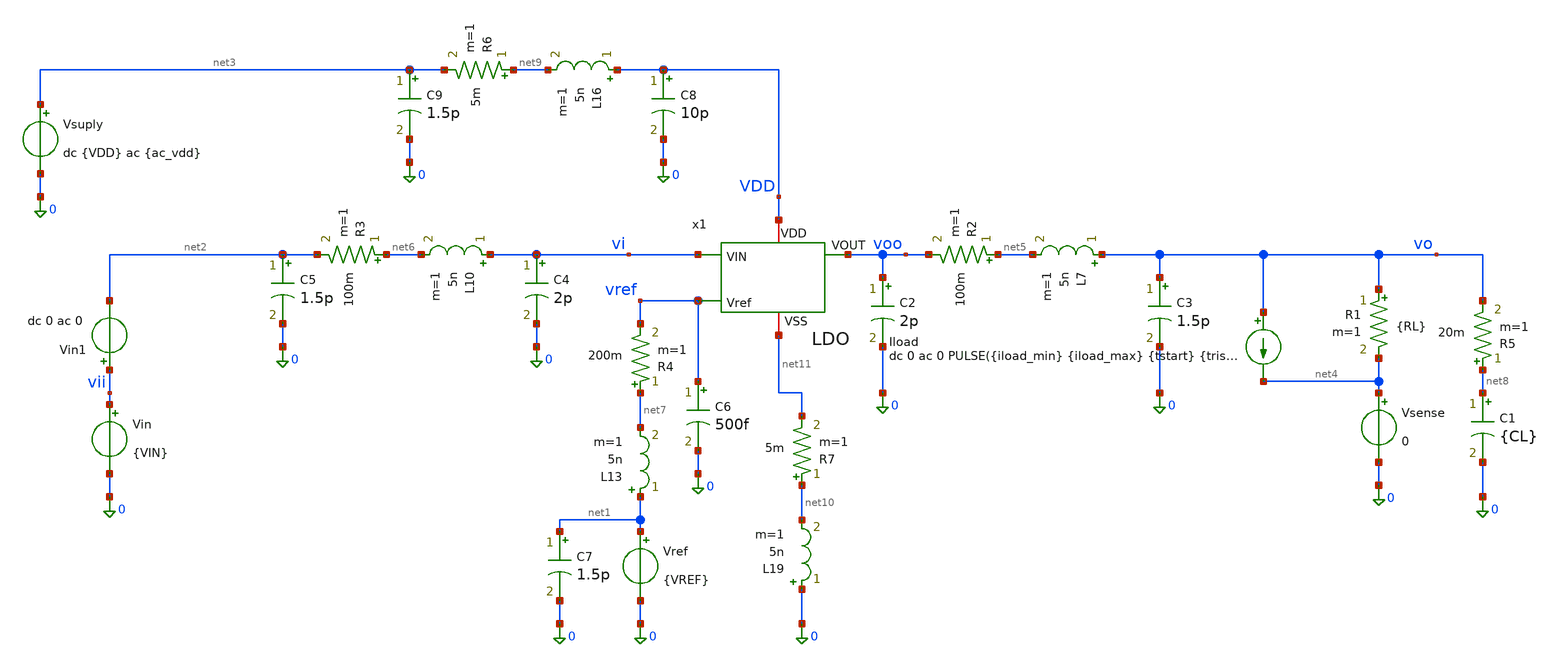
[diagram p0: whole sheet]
** sch_path: xschem/LDO_Top/ldo_tb.sch
**.subckt ldo_tb
Vsuply net3 0 dc {VDD} ac {ac_vdd}
Vref net1 0 {VREF}
Vin vii 0 {VIN}
R1 vo net4 {RL} m=1
C1 net8 0 {CL} m=1
Iload vo net4 dc 0 ac 0 PULSE({iload_min} {iload_max} {tstart} {trise} {tfall} {twidth} {tperiod})
Vsense net4 0 0
Vin1 vii net2 dc 0 ac 0
x1 vi voo VDD vref net11 LDO
C2 voo 0 2p m=1
R2 net5 voo 100m m=1
L7 vo net5 5n m=1
C3 vo 0 1.5p m=1
L10 vi net6 5n m=1
C4 vi 0 2p m=1
C5 net2 0 1.5p m=1
R3 net6 net2 100m m=1
L13 net1 net7 5n m=1
R4 net7 vref 200m m=1
C6 vref 0 500f m=1
C7 net1 0 1.5p m=1
R5 net8 vo 20m m=1
L16 VDD net9 5n m=1
C8 VDD 0 10p m=1
C9 net3 0 1.5p m=1
R6 net9 net3 5m m=1
L19 0 net10 5n m=1
R7 net10 net11 5m m=1
**** begin user architecture code









.lib /foss/pdks/sky130A/libs.tech/ngspice/sky130.lib.spice ff_lh
.option temp=-40
.param VDD = 1.98

.option num_threads=8

.param rsh_var = agauss(0, 0.005, 1)


* Forzar un punto de partida para ayudar a la convergencia
.nodeset V(VO)=1.2
.nodeset V(x1.Vre)=0.6




**parametros_ldo

.param VREF = 0.6
.param VIN = '1*VDD-0.3'
.param RL = 1200
.param CL = 1u
.param tsim = 2m

* Parámetros para la prueba de carga del LDO
.param iload_min = 1u
.param iload_max = 5m
.param tstart   = 30u
.param trise    = 100n
.param tfall    = 100n
.param twidth   = 100u
.param tperiod  = 200u

.param tsim = '3*tperiod'

.param ac_iprobe = 1
.param ac_vdd = 0

* --- Clamp SOLO de simulación (evita soluciones DC falsas de cientos de V) ---
* Diodo a tierra: conduce si vo baja de -0.2 V
Dclpn 0 vo dclamp_tb
* Diodo a una fuente de 5 V: conduce si vo sube de 5.7 V
Dclpp vo vclp dclamp_tb
* Fuente de referencia para el clamp superior
Dclpn2 0 x1.vre dclamp_tb
Dclpp2 x1.vre vclp dclamp_tb
Vclp vclp 0 5
* Modelo del diodo (fuga ~fA, sin capacitancia: no altera AC ni transitorio)
.model dclamp_tb D(IS=1e-15 N=1)









.control
let tperiod  = 200u
let tsim = '3*tperiod'


* =========================================================
* 2. AC (Estabilidad) -> Genera plot ac1
* =========================================================

ac dec 10 1 1G


let T_loop = v(x1.vre) / v(x1.vre2)
let ldb = vdb(T_loop)
let fase = vp(T_loop) * 180 / pi

write LDO_ac_estability.raw
meas ac ugb WHEN ldb = 0.0
meas ac fase_ugb FIND fase WHEN ldb = 0.0
let margen_fase = fase_ugb
meas ac ganancia_banda_plana find ldb at=1

* =========================================================
* 3. AC (PSRR) -> Genera plot ac2
* =========================================================
alterparam ac_iprobe = 0
alterparam ac_vdd = 1
reset

ac dec 10 10 1G


let psrr1 = v(vdd)/v(vo)
let psrr_db = vdb(psrr1)
write LDO_ac_psrr.raw
meas ac gananciaPSRR_1   find psrr_db at=10
meas ac gananciaPSRR_1k  find psrr_db at=1k
meas ac gananciaPSRR_10k find psrr_db at=10k
meas ac gananciaPSRR_1M  find psrr_db at=1Meg

* =========================================================
* 4. TRANSIENTE (Line Regulation) -> Genera plot tran1
* =========================================================
alterparam ac_iprobe = 0
alterparam ac_vdd = 0
reset

alter @Vin[pwl] = [ 0 1.4 1m 1.8 ]
alter @Iload[pwl] = [ 0 1u 1m 1u ]

tran 1u 1m
write LDO_dc_line.raw

let t_line_ini = 40u
let t_line_fin = 950u

meas tran voline_max MAX v(vo) from=$&t_line_ini to=$&t_line_fin
meas tran voline_min MIN v(vo) from=$&t_line_ini to=$&t_line_fin
let line_regulation_mV = (voline_max - voline_min)*1000
meas tran salida_line avg v(vo) from=$&t_line_ini to=$&t_line_fin
* =========================================================

* 1. TRANSIENTE (Overshoot y Undershoot) -> Genera plot tran2
* =========================================================
alterparam ac_iprobe = 0
alterparam ac_vdd = 0
alterparam RL = 240e9
reset

tran 1u $&tsim
write LDO_tran_picos.raw

let t_ignorar = 150u

meas tran v_estable_ligera FIND v(vo) AT=270u
meas tran v_estable_pesada FIND v(vo) AT=180u
meas tran vo_max MAX v(vo) from=$&t_ignorar to=$&tsim
meas tran vo_min MIN v(vo) from=$&t_ignorar to=$&tsim

let undershoot_mV = (v_estable_ligera - vo_min) * 1e3
let overshoot_mV = (vo_max - v_estable_pesada) * 1e3
meas tran salida_tran avg v(vo) from=$&t_ignorar to=$&tsim


* =========================================================
* 5. TRANSIENTE (Load Regulation) -> Genera plot tran3
* =========================================================
alterparam RL = 240e9
reset
alter @Iload[pwl] = [ 0 1u 1m 5m ]

tran 1u 1m
write LDO_dc_load.raw

meas tran vout_light FIND v(vo) AT=40u
meas tran vout_heavy FIND v(vo) AT=1m
let load_regulation_mV = (vout_light - vout_heavy) * 1000

* =========================================================
* 6. TRANSIENTE (Dropout) -> Genera plot tran4
* =========================================================
alterparam RL = 240
reset
alter @Vin[pwl] = [ 0 2 1m 0 ]
alter @Iload[pwl] = [ 0 1u 1m 1u ]

tran 1u 1m
write LDO_dc_dropout.raw

meas tran vout_nom FIND v(vo) AT=225u
let vout_target = vout_nom * 0.90
meas tran vin_do FIND v(vi) WHEN v(vo) = vout_target fall=1
let dropout_mV = (vin_do - vout_target) * 1e3

* =========================================================
* IMPRESION DE TODOS LOS RESULTADOS CON SETPLOT
* =========================================================

echo '--- RESULTADOS DE TRANSIENTE ---'
setplot tran3
print undershoot_mV overshoot_mV v_estable_ligera v_estable_pesada salida_tran

echo '--- RESULTADOS AC (ESTABILIDAD) ---'
setplot ac1
print ugb fase_ugb margen_fase ganancia_banda_plana

echo '--- RESULTADOS AC (PSRR) ---'
setplot ac2
print gananciaPSRR_1 gananciaPSRR_1k gananciaPSRR_10k gananciaPSRR_1M

echo '--- RESULTADOS REGULACIONES Y DROPOUT ---'
echo '>> Line Regulation'
setplot tran2
print line_regulation_mV salida_line

echo '>> Load Regulation'
setplot tran4
print load_regulation_mV

echo '>> Dropout'
setplot tran5
print dropout_mV vin_do vout_target

.endc






















.control



alterparam RL = 1200
alterparam ac_iprobe = 0
alterparam ac_vdd = 0

reset

*  Punto de Operación (.OP)

save all


save @m.x1.xM1.msky130_fd_pr__pfet_01v8_lvt[gm]
save @m.x1.xM1.msky130_fd_pr__pfet_01v8_lvt[gds]
save @m.x1.xM1.msky130_fd_pr__pfet_01v8_lvt[id]
save @m.x1.xM1.msky130_fd_pr__pfet_01v8_lvt[vgs]
save @m.x1.xM1.msky130_fd_pr__pfet_01v8_lvt[vds]
save @m.x1.xM1.msky130_fd_pr__pfet_01v8_lvt[vth]
save @m.x1.xM1.msky130_fd_pr__pfet_01v8_lvt[vdsat]




save @m.x1.x1.xMr.msky130_fd_pr__pfet_01v8_lvt[gm]
save @m.x1.x1.xMr.msky130_fd_pr__pfet_01v8_lvt[gds]
save @m.x1.x1.xMr.msky130_fd_pr__pfet_01v8_lvt[id]
save @m.x1.x1.xMr.msky130_fd_pr__pfet_01v8_lvt[vgs]
save @m.x1.x1.xMr.msky130_fd_pr__pfet_01v8_lvt[vds]
save @m.x1.x1.xMr.msky130_fd_pr__pfet_01v8_lvt[vth]
save @m.x1.x1.xMr.msky130_fd_pr__pfet_01v8_lvt[vdsat]

save @m.x1.x1.xMnref.msky130_fd_pr__nfet_01v8[gm]
save @m.x1.x1.xMnref.msky130_fd_pr__nfet_01v8[gds]
save @m.x1.x1.xMnref.msky130_fd_pr__nfet_01v8[id]
save @m.x1.x1.xMnref.msky130_fd_pr__nfet_01v8[vgs]
save @m.x1.x1.xMnref.msky130_fd_pr__nfet_01v8[vds]
save @m.x1.x1.xMnref.msky130_fd_pr__nfet_01v8[vth]
save @m.x1.x1.xMnref.msky130_fd_pr__nfet_01v8[vdsat]

save @m.x1.xMnl.msky130_fd_pr__nfet_01v8[gm]
save @m.x1.xMnl.msky130_fd_pr__nfet_01v8[gds]
save @m.x1.xMnl.msky130_fd_pr__nfet_01v8[id]
save @m.x1.xMnl.msky130_fd_pr__nfet_01v8[vgs]
save @m.x1.xMnl.msky130_fd_pr__nfet_01v8[vds]
save @m.x1.xMnl.msky130_fd_pr__nfet_01v8[vth]
save @m.x1.xMnl.msky130_fd_pr__nfet_01v8[vdsat]



* --- Etapa Diferencial (Núcleo del OTA) ---

* Mrc1 (pfet_01v8_lvt)
save @m.x1.x1.xMrc1.msky130_fd_pr__pfet_01v8_lvt[gm]
save @m.x1.x1.xMrc1.msky130_fd_pr__pfet_01v8_lvt[gds]
save @m.x1.x1.xMrc1.msky130_fd_pr__pfet_01v8_lvt[id]
save @m.x1.x1.xMrc1.msky130_fd_pr__pfet_01v8_lvt[vgs]
save @m.x1.x1.xMrc1.msky130_fd_pr__pfet_01v8_lvt[vds]
save @m.x1.x1.xMrc1.msky130_fd_pr__pfet_01v8_lvt[vth]
save @m.x1.x1.xMrc1.msky130_fd_pr__pfet_01v8_lvt[vdsat]

* Mn (pfet_01v8)
save @m.x1.x1.xMn.msky130_fd_pr__pfet_01v8_lvt[gm]
save @m.x1.x1.xMn.msky130_fd_pr__pfet_01v8_lvt[gds]
save @m.x1.x1.xMn.msky130_fd_pr__pfet_01v8_lvt[id]
save @m.x1.x1.xMn.msky130_fd_pr__pfet_01v8_lvt[vgs]
save @m.x1.x1.xMn.msky130_fd_pr__pfet_01v8_lvt[vds]
save @m.x1.x1.xMn.msky130_fd_pr__pfet_01v8_lvt[vth]
save @m.x1.x1.xMn.msky130_fd_pr__pfet_01v8_lvt[vdsat]

* Mp (pfet_01v8)
save @m.x1.x1.xMp.msky130_fd_pr__pfet_01v8_lvt[gm]
save @m.x1.x1.xMp.msky130_fd_pr__pfet_01v8_lvt[gds]
save @m.x1.x1.xMp.msky130_fd_pr__pfet_01v8_lvt[id]
save @m.x1.x1.xMp.msky130_fd_pr__pfet_01v8_lvt[vgs]
save @m.x1.x1.xMp.msky130_fd_pr__pfet_01v8_lvt[vds]
save @m.x1.x1.xMp.msky130_fd_pr__pfet_01v8_lvt[vth]
save @m.x1.x1.xMp.msky130_fd_pr__pfet_01v8_lvt[vdsat]

* Mnr (nfet_01v8)
save @m.x1.x1.xMnr.msky130_fd_pr__nfet_01v8[gm]
save @m.x1.x1.xMnr.msky130_fd_pr__nfet_01v8[gds]
save @m.x1.x1.xMnr.msky130_fd_pr__nfet_01v8[id]
save @m.x1.x1.xMnr.msky130_fd_pr__nfet_01v8[vgs]
save @m.x1.x1.xMnr.msky130_fd_pr__nfet_01v8[vds]
save @m.x1.x1.xMnr.msky130_fd_pr__nfet_01v8[vth]
save @m.x1.x1.xMnr.msky130_fd_pr__nfet_01v8[vdsat]

* Mpr (nfet_01v8)
save @m.x1.x1.xMpr.msky130_fd_pr__nfet_01v8[gm]
save @m.x1.x1.xMpr.msky130_fd_pr__nfet_01v8[gds]
save @m.x1.x1.xMpr.msky130_fd_pr__nfet_01v8[id]
save @m.x1.x1.xMpr.msky130_fd_pr__nfet_01v8[vgs]
save @m.x1.x1.xMpr.msky130_fd_pr__nfet_01v8[vds]
save @m.x1.x1.xMpr.msky130_fd_pr__nfet_01v8[vth]
save @m.x1.x1.xMpr.msky130_fd_pr__nfet_01v8[vdsat]


* --- Etapa de Salida ---

* Mrc2 (pfet_01v8_lvt)
save @m.x1.x1.xMrc2.msky130_fd_pr__pfet_01v8_lvt[gm]
save @m.x1.x1.xMrc2.msky130_fd_pr__pfet_01v8_lvt[gds]
save @m.x1.x1.xMrc2.msky130_fd_pr__pfet_01v8_lvt[id]
save @m.x1.x1.xMrc2.msky130_fd_pr__pfet_01v8_lvt[vgs]
save @m.x1.x1.xMrc2.msky130_fd_pr__pfet_01v8_lvt[vds]
save @m.x1.x1.xMrc2.msky130_fd_pr__pfet_01v8_lvt[vth]
save @m.x1.x1.xMrc2.msky130_fd_pr__pfet_01v8_lvt[vdsat]

* Mo (nfet_01v8)
save @m.x1.x1.xMo.msky130_fd_pr__nfet_01v8[gm]
save @m.x1.x1.xMo.msky130_fd_pr__nfet_01v8[gds]
save @m.x1.x1.xMo.msky130_fd_pr__nfet_01v8[id]
save @m.x1.x1.xMo.msky130_fd_pr__nfet_01v8[vgs]
save @m.x1.x1.xMo.msky130_fd_pr__nfet_01v8[vds]
save @m.x1.x1.xMo.msky130_fd_pr__nfet_01v8[vth]
save @m.x1.x1.xMo.msky130_fd_pr__nfet_01v8[vdsat]


op
set filetype=ascii
write LDO_op.raw

















.endc






**** end user architecture code
**.ends
.end
